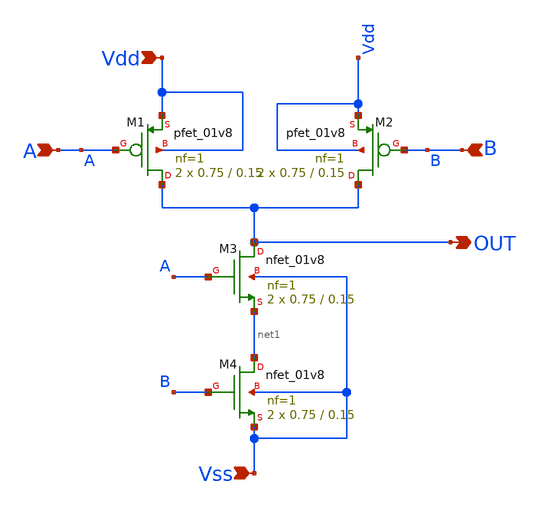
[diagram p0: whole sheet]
** sch_path: icdesign/sch/NAND/NAND.sch
**.subckt NAND Vss Vdd A B OUT
*.ipin Vss
*.ipin Vdd
*.ipin A
*.ipin B
*.opin OUT
XM1 OUT A Vdd Vdd sky130_fd_pr__pfet_01v8 L=0.15 W=0.75 nf=1 ad='int((nf+1)/2) * W/nf * 0.29' as='int((nf+2)/2) * W/nf * 0.29'
+ pd='2*int((nf+1)/2) * (W/nf + 0.29)' ps='2*int((nf+2)/2) * (W/nf + 0.29)' nrd='0.29 / W' nrs='0.29 / W'
+ sa=0 sb=0 sd=0 mult=2 m=2
XM2 OUT B Vdd Vdd sky130_fd_pr__pfet_01v8 L=0.15 W=0.75 nf=1 ad='int((nf+1)/2) * W/nf * 0.29' as='int((nf+2)/2) * W/nf * 0.29'
+ pd='2*int((nf+1)/2) * (W/nf + 0.29)' ps='2*int((nf+2)/2) * (W/nf + 0.29)' nrd='0.29 / W' nrs='0.29 / W'
+ sa=0 sb=0 sd=0 mult=2 m=2
XM3 OUT A net1 Vss sky130_fd_pr__nfet_01v8 L=0.15 W=0.75 nf=1 ad='int((nf+1)/2) * W/nf * 0.29' as='int((nf+2)/2) * W/nf * 0.29'
+ pd='2*int((nf+1)/2) * (W/nf + 0.29)' ps='2*int((nf+2)/2) * (W/nf + 0.29)' nrd='0.29 / W' nrs='0.29 / W'
+ sa=0 sb=0 sd=0 mult=2 m=2
XM4 net1 B Vss Vss sky130_fd_pr__nfet_01v8 L=0.15 W=0.75 nf=1 ad='int((nf+1)/2) * W/nf * 0.29' as='int((nf+2)/2) * W/nf * 0.29'
+ pd='2*int((nf+1)/2) * (W/nf + 0.29)' ps='2*int((nf+2)/2) * (W/nf + 0.29)' nrd='0.29 / W' nrs='0.29 / W'
+ sa=0 sb=0 sd=0 mult=2 m=2
**.ends
.end
